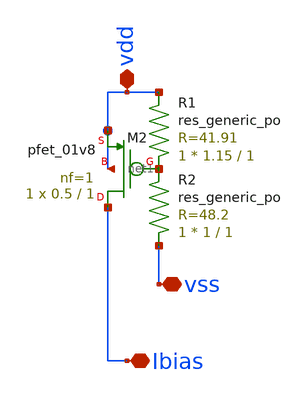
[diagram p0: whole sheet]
** sch_path: Neuron/ultralif/syn_bias.sch
**.subckt syn_bias vss vdd Ibias
*.iopin vss
*.iopin vdd
*.iopin Ibias
XM2 Ibias net1 vdd vdd sky130_fd_pr__pfet_01v8 L=1 W=0.5 nf=1 ad='int((nf+1)/2) * W/nf * 0.29' as='int((nf+2)/2) * W/nf * 0.29'
+ pd='2*int((nf+1)/2) * (W/nf + 0.29)' ps='2*int((nf+2)/2) * (W/nf + 0.29)' nrd='0.29 / W' nrs='0.29 / W'
+ sa=0 sb=0 sd=0 mult=1 m=1
XR1 net1 vdd sky130_fd_pr__res_generic_po W=1.15 L=1 m=1
XR2 vss net1 sky130_fd_pr__res_generic_po W=1 L=1 m=1
**.ends
.end
